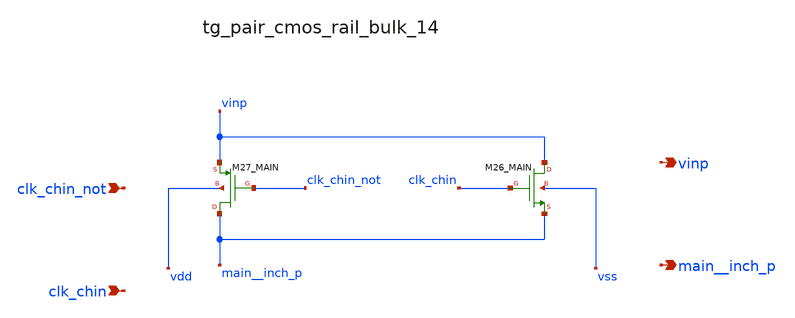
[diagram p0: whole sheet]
** sch_path: analog-db/raw/ia_004_fan_chopper_rrl/hier/blocks/tg_pair_cmos_rail_bulk_14.sch
**.subckt tg_pair_cmos_rail_bulk_14 clk_chin_not clk_chin vinp main__inch_p
*.ipin clk_chin_not
*.ipin clk_chin
*.opin vinp
*.opin main__inch_p
XM26_MAIN vinp clk_chin main__inch_p vss sg13_lv_nmos w=x_dut_xm26_main_w l=x_dut_xm26_main_l ng=1
+ m=x_dut_xm26_main_m
XM27_MAIN main__inch_p clk_chin_not vinp vdd sg13_lv_pmos w=x_dut_xm27_main_w l=x_dut_xm27_main_l
+ ng=1 m=x_dut_xm27_main_m
**.ends
.end
